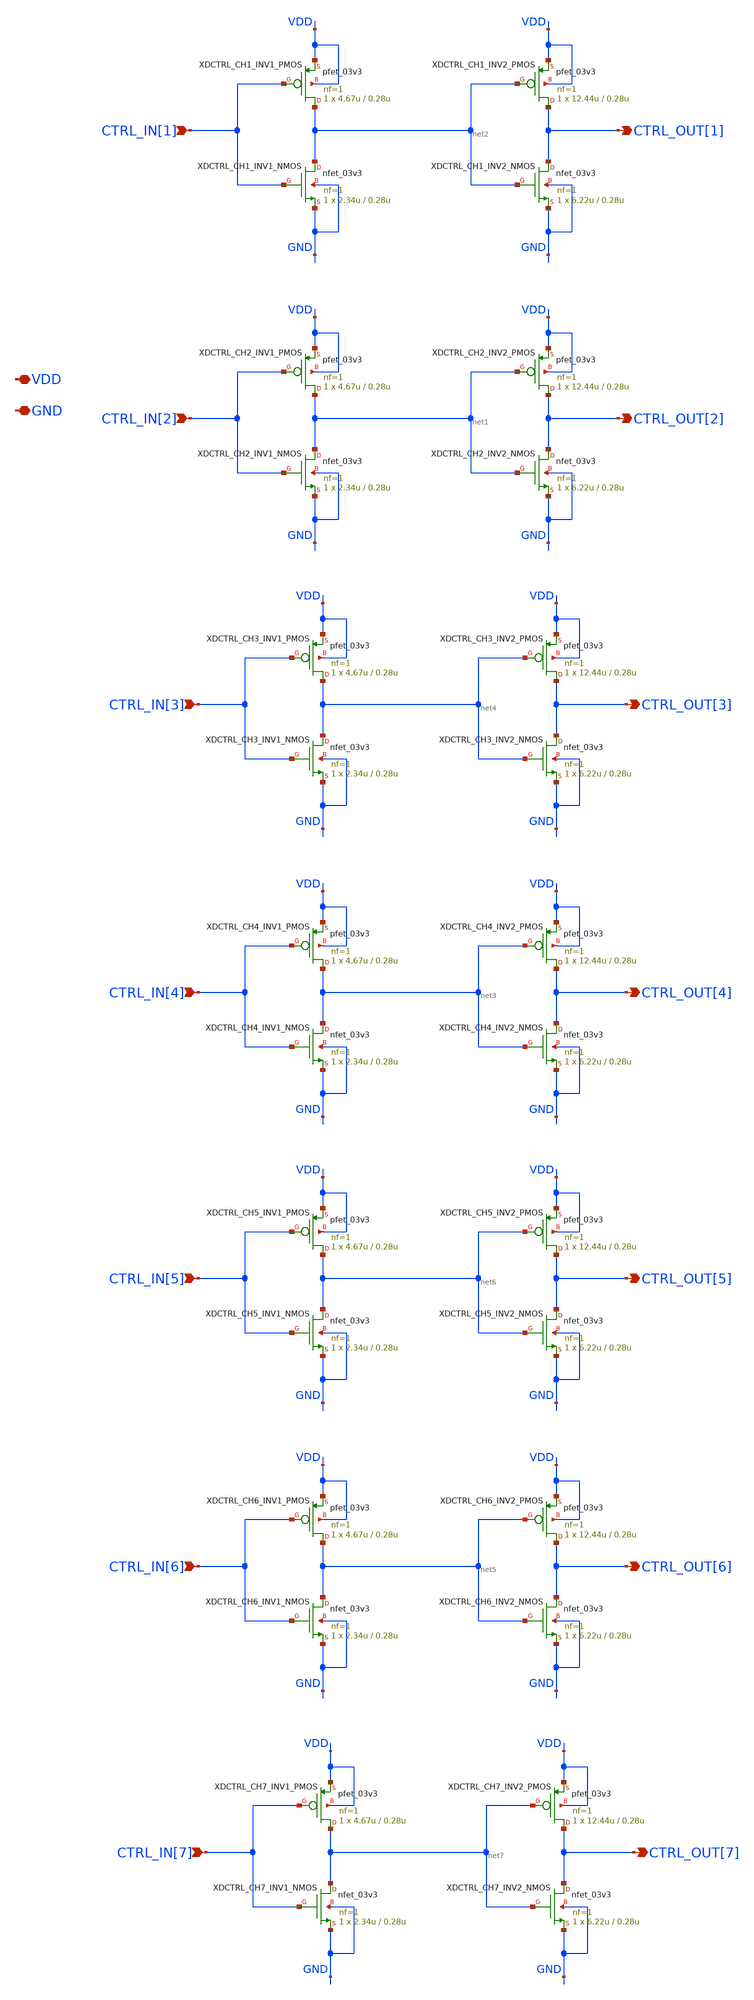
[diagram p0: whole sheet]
** sch_path: verification/a44_w5p29_trans_driver/01_CURRENT_CIRCUIT_FILES/xschem/A44_CONVERSION_BUFFER.sch
**.subckt A44_CONVERSION_BUFFER CTRL_IN[2] CTRL_OUT[2] VDD GND CTRL_IN[1] CTRL_OUT[1] CTRL_IN[4]
*+ CTRL_OUT[4] CTRL_IN[3] CTRL_OUT[3] CTRL_IN[6] CTRL_OUT[6] CTRL_IN[5] CTRL_OUT[5] CTRL_IN[7] CTRL_OUT[7]
*.ipin CTRL_IN[2]
*.opin CTRL_OUT[2]
*.iopin VDD
*.iopin GND
*.ipin CTRL_IN[1]
*.opin CTRL_OUT[1]
*.ipin CTRL_IN[4]
*.opin CTRL_OUT[4]
*.ipin CTRL_IN[3]
*.opin CTRL_OUT[3]
*.ipin CTRL_IN[6]
*.opin CTRL_OUT[6]
*.ipin CTRL_IN[5]
*.opin CTRL_OUT[5]
*.ipin CTRL_IN[7]
*.opin CTRL_OUT[7]
XDCTRL_CH2_INV1_NMOS net1 CTRL_IN[2] GND GND nfet_03v3 L=0.28u W=2.34u nf=1 ad='int((nf+1)/2) * W/nf * 0.18u'
+ as='int((nf+2)/2) * W/nf * 0.18u' pd='2*int((nf+1)/2) * (W/nf + 0.18u)' ps='2*int((nf+2)/2) * (W/nf + 0.18u)'
+ nrd='0.18u / W' nrs='0.18u / W' sa=0 sb=0 sd=0 m=1
XDCTRL_CH2_INV1_PMOS net1 CTRL_IN[2] VDD VDD pfet_03v3 L=0.28u W=4.67u nf=1 ad='int((nf+1)/2) * W/nf * 0.18u'
+ as='int((nf+2)/2) * W/nf * 0.18u' pd='2*int((nf+1)/2) * (W/nf + 0.18u)' ps='2*int((nf+2)/2) * (W/nf + 0.18u)'
+ nrd='0.18u / W' nrs='0.18u / W' sa=0 sb=0 sd=0 m=1
XDCTRL_CH2_INV2_NMOS CTRL_OUT[2] net1 GND GND nfet_03v3 L=0.28u W=6.22u nf=1 ad='int((nf+1)/2) * W/nf * 0.18u'
+ as='int((nf+2)/2) * W/nf * 0.18u' pd='2*int((nf+1)/2) * (W/nf + 0.18u)' ps='2*int((nf+2)/2) * (W/nf + 0.18u)'
+ nrd='0.18u / W' nrs='0.18u / W' sa=0 sb=0 sd=0 m=1
XDCTRL_CH2_INV2_PMOS CTRL_OUT[2] net1 VDD VDD pfet_03v3 L=0.28u W=12.44u nf=1 ad='int((nf+1)/2) * W/nf * 0.18u'
+ as='int((nf+2)/2) * W/nf * 0.18u' pd='2*int((nf+1)/2) * (W/nf + 0.18u)' ps='2*int((nf+2)/2) * (W/nf + 0.18u)'
+ nrd='0.18u / W' nrs='0.18u / W' sa=0 sb=0 sd=0 m=1
XDCTRL_CH1_INV1_NMOS net2 CTRL_IN[1] GND GND nfet_03v3 L=0.28u W=2.34u nf=1 ad='int((nf+1)/2) * W/nf * 0.18u'
+ as='int((nf+2)/2) * W/nf * 0.18u' pd='2*int((nf+1)/2) * (W/nf + 0.18u)' ps='2*int((nf+2)/2) * (W/nf + 0.18u)'
+ nrd='0.18u / W' nrs='0.18u / W' sa=0 sb=0 sd=0 m=1
XDCTRL_CH1_INV1_PMOS net2 CTRL_IN[1] VDD VDD pfet_03v3 L=0.28u W=4.67u nf=1 ad='int((nf+1)/2) * W/nf * 0.18u'
+ as='int((nf+2)/2) * W/nf * 0.18u' pd='2*int((nf+1)/2) * (W/nf + 0.18u)' ps='2*int((nf+2)/2) * (W/nf + 0.18u)'
+ nrd='0.18u / W' nrs='0.18u / W' sa=0 sb=0 sd=0 m=1
XDCTRL_CH1_INV2_NMOS CTRL_OUT[1] net2 GND GND nfet_03v3 L=0.28u W=6.22u nf=1 ad='int((nf+1)/2) * W/nf * 0.18u'
+ as='int((nf+2)/2) * W/nf * 0.18u' pd='2*int((nf+1)/2) * (W/nf + 0.18u)' ps='2*int((nf+2)/2) * (W/nf + 0.18u)'
+ nrd='0.18u / W' nrs='0.18u / W' sa=0 sb=0 sd=0 m=1
XDCTRL_CH1_INV2_PMOS CTRL_OUT[1] net2 VDD VDD pfet_03v3 L=0.28u W=12.44u nf=1 ad='int((nf+1)/2) * W/nf * 0.18u'
+ as='int((nf+2)/2) * W/nf * 0.18u' pd='2*int((nf+1)/2) * (W/nf + 0.18u)' ps='2*int((nf+2)/2) * (W/nf + 0.18u)'
+ nrd='0.18u / W' nrs='0.18u / W' sa=0 sb=0 sd=0 m=1
XDCTRL_CH4_INV1_NMOS net3 CTRL_IN[4] GND GND nfet_03v3 L=0.28u W=2.34u nf=1 ad='int((nf+1)/2) * W/nf * 0.18u'
+ as='int((nf+2)/2) * W/nf * 0.18u' pd='2*int((nf+1)/2) * (W/nf + 0.18u)' ps='2*int((nf+2)/2) * (W/nf + 0.18u)'
+ nrd='0.18u / W' nrs='0.18u / W' sa=0 sb=0 sd=0 m=1
XDCTRL_CH4_INV1_PMOS net3 CTRL_IN[4] VDD VDD pfet_03v3 L=0.28u W=4.67u nf=1 ad='int((nf+1)/2) * W/nf * 0.18u'
+ as='int((nf+2)/2) * W/nf * 0.18u' pd='2*int((nf+1)/2) * (W/nf + 0.18u)' ps='2*int((nf+2)/2) * (W/nf + 0.18u)'
+ nrd='0.18u / W' nrs='0.18u / W' sa=0 sb=0 sd=0 m=1
XDCTRL_CH4_INV2_NMOS CTRL_OUT[4] net3 GND GND nfet_03v3 L=0.28u W=6.22u nf=1 ad='int((nf+1)/2) * W/nf * 0.18u'
+ as='int((nf+2)/2) * W/nf * 0.18u' pd='2*int((nf+1)/2) * (W/nf + 0.18u)' ps='2*int((nf+2)/2) * (W/nf + 0.18u)'
+ nrd='0.18u / W' nrs='0.18u / W' sa=0 sb=0 sd=0 m=1
XDCTRL_CH4_INV2_PMOS CTRL_OUT[4] net3 VDD VDD pfet_03v3 L=0.28u W=12.44u nf=1 ad='int((nf+1)/2) * W/nf * 0.18u'
+ as='int((nf+2)/2) * W/nf * 0.18u' pd='2*int((nf+1)/2) * (W/nf + 0.18u)' ps='2*int((nf+2)/2) * (W/nf + 0.18u)'
+ nrd='0.18u / W' nrs='0.18u / W' sa=0 sb=0 sd=0 m=1
XDCTRL_CH3_INV1_NMOS net4 CTRL_IN[3] GND GND nfet_03v3 L=0.28u W=2.34u nf=1 ad='int((nf+1)/2) * W/nf * 0.18u'
+ as='int((nf+2)/2) * W/nf * 0.18u' pd='2*int((nf+1)/2) * (W/nf + 0.18u)' ps='2*int((nf+2)/2) * (W/nf + 0.18u)'
+ nrd='0.18u / W' nrs='0.18u / W' sa=0 sb=0 sd=0 m=1
XDCTRL_CH3_INV1_PMOS net4 CTRL_IN[3] VDD VDD pfet_03v3 L=0.28u W=4.67u nf=1 ad='int((nf+1)/2) * W/nf * 0.18u'
+ as='int((nf+2)/2) * W/nf * 0.18u' pd='2*int((nf+1)/2) * (W/nf + 0.18u)' ps='2*int((nf+2)/2) * (W/nf + 0.18u)'
+ nrd='0.18u / W' nrs='0.18u / W' sa=0 sb=0 sd=0 m=1
XDCTRL_CH3_INV2_NMOS CTRL_OUT[3] net4 GND GND nfet_03v3 L=0.28u W=6.22u nf=1 ad='int((nf+1)/2) * W/nf * 0.18u'
+ as='int((nf+2)/2) * W/nf * 0.18u' pd='2*int((nf+1)/2) * (W/nf + 0.18u)' ps='2*int((nf+2)/2) * (W/nf + 0.18u)'
+ nrd='0.18u / W' nrs='0.18u / W' sa=0 sb=0 sd=0 m=1
XDCTRL_CH3_INV2_PMOS CTRL_OUT[3] net4 VDD VDD pfet_03v3 L=0.28u W=12.44u nf=1 ad='int((nf+1)/2) * W/nf * 0.18u'
+ as='int((nf+2)/2) * W/nf * 0.18u' pd='2*int((nf+1)/2) * (W/nf + 0.18u)' ps='2*int((nf+2)/2) * (W/nf + 0.18u)'
+ nrd='0.18u / W' nrs='0.18u / W' sa=0 sb=0 sd=0 m=1
XDCTRL_CH6_INV1_NMOS net5 CTRL_IN[6] GND GND nfet_03v3 L=0.28u W=2.34u nf=1 ad='int((nf+1)/2) * W/nf * 0.18u'
+ as='int((nf+2)/2) * W/nf * 0.18u' pd='2*int((nf+1)/2) * (W/nf + 0.18u)' ps='2*int((nf+2)/2) * (W/nf + 0.18u)'
+ nrd='0.18u / W' nrs='0.18u / W' sa=0 sb=0 sd=0 m=1
XDCTRL_CH6_INV1_PMOS net5 CTRL_IN[6] VDD VDD pfet_03v3 L=0.28u W=4.67u nf=1 ad='int((nf+1)/2) * W/nf * 0.18u'
+ as='int((nf+2)/2) * W/nf * 0.18u' pd='2*int((nf+1)/2) * (W/nf + 0.18u)' ps='2*int((nf+2)/2) * (W/nf + 0.18u)'
+ nrd='0.18u / W' nrs='0.18u / W' sa=0 sb=0 sd=0 m=1
XDCTRL_CH6_INV2_NMOS CTRL_OUT[6] net5 GND GND nfet_03v3 L=0.28u W=6.22u nf=1 ad='int((nf+1)/2) * W/nf * 0.18u'
+ as='int((nf+2)/2) * W/nf * 0.18u' pd='2*int((nf+1)/2) * (W/nf + 0.18u)' ps='2*int((nf+2)/2) * (W/nf + 0.18u)'
+ nrd='0.18u / W' nrs='0.18u / W' sa=0 sb=0 sd=0 m=1
XDCTRL_CH6_INV2_PMOS CTRL_OUT[6] net5 VDD VDD pfet_03v3 L=0.28u W=12.44u nf=1 ad='int((nf+1)/2) * W/nf * 0.18u'
+ as='int((nf+2)/2) * W/nf * 0.18u' pd='2*int((nf+1)/2) * (W/nf + 0.18u)' ps='2*int((nf+2)/2) * (W/nf + 0.18u)'
+ nrd='0.18u / W' nrs='0.18u / W' sa=0 sb=0 sd=0 m=1
XDCTRL_CH5_INV1_NMOS net6 CTRL_IN[5] GND GND nfet_03v3 L=0.28u W=2.34u nf=1 ad='int((nf+1)/2) * W/nf * 0.18u'
+ as='int((nf+2)/2) * W/nf * 0.18u' pd='2*int((nf+1)/2) * (W/nf + 0.18u)' ps='2*int((nf+2)/2) * (W/nf + 0.18u)'
+ nrd='0.18u / W' nrs='0.18u / W' sa=0 sb=0 sd=0 m=1
XDCTRL_CH5_INV1_PMOS net6 CTRL_IN[5] VDD VDD pfet_03v3 L=0.28u W=4.67u nf=1 ad='int((nf+1)/2) * W/nf * 0.18u'
+ as='int((nf+2)/2) * W/nf * 0.18u' pd='2*int((nf+1)/2) * (W/nf + 0.18u)' ps='2*int((nf+2)/2) * (W/nf + 0.18u)'
+ nrd='0.18u / W' nrs='0.18u / W' sa=0 sb=0 sd=0 m=1
XDCTRL_CH5_INV2_NMOS CTRL_OUT[5] net6 GND GND nfet_03v3 L=0.28u W=6.22u nf=1 ad='int((nf+1)/2) * W/nf * 0.18u'
+ as='int((nf+2)/2) * W/nf * 0.18u' pd='2*int((nf+1)/2) * (W/nf + 0.18u)' ps='2*int((nf+2)/2) * (W/nf + 0.18u)'
+ nrd='0.18u / W' nrs='0.18u / W' sa=0 sb=0 sd=0 m=1
XDCTRL_CH5_INV2_PMOS CTRL_OUT[5] net6 VDD VDD pfet_03v3 L=0.28u W=12.44u nf=1 ad='int((nf+1)/2) * W/nf * 0.18u'
+ as='int((nf+2)/2) * W/nf * 0.18u' pd='2*int((nf+1)/2) * (W/nf + 0.18u)' ps='2*int((nf+2)/2) * (W/nf + 0.18u)'
+ nrd='0.18u / W' nrs='0.18u / W' sa=0 sb=0 sd=0 m=1
XDCTRL_CH7_INV1_NMOS net7 CTRL_IN[7] GND GND nfet_03v3 L=0.28u W=2.34u nf=1 ad='int((nf+1)/2) * W/nf * 0.18u'
+ as='int((nf+2)/2) * W/nf * 0.18u' pd='2*int((nf+1)/2) * (W/nf + 0.18u)' ps='2*int((nf+2)/2) * (W/nf + 0.18u)'
+ nrd='0.18u / W' nrs='0.18u / W' sa=0 sb=0 sd=0 m=1
XDCTRL_CH7_INV1_PMOS net7 CTRL_IN[7] VDD VDD pfet_03v3 L=0.28u W=4.67u nf=1 ad='int((nf+1)/2) * W/nf * 0.18u'
+ as='int((nf+2)/2) * W/nf * 0.18u' pd='2*int((nf+1)/2) * (W/nf + 0.18u)' ps='2*int((nf+2)/2) * (W/nf + 0.18u)'
+ nrd='0.18u / W' nrs='0.18u / W' sa=0 sb=0 sd=0 m=1
XDCTRL_CH7_INV2_NMOS CTRL_OUT[7] net7 GND GND nfet_03v3 L=0.28u W=6.22u nf=1 ad='int((nf+1)/2) * W/nf * 0.18u'
+ as='int((nf+2)/2) * W/nf * 0.18u' pd='2*int((nf+1)/2) * (W/nf + 0.18u)' ps='2*int((nf+2)/2) * (W/nf + 0.18u)'
+ nrd='0.18u / W' nrs='0.18u / W' sa=0 sb=0 sd=0 m=1
XDCTRL_CH7_INV2_PMOS CTRL_OUT[7] net7 VDD VDD pfet_03v3 L=0.28u W=12.44u nf=1 ad='int((nf+1)/2) * W/nf * 0.18u'
+ as='int((nf+2)/2) * W/nf * 0.18u' pd='2*int((nf+1)/2) * (W/nf + 0.18u)' ps='2*int((nf+2)/2) * (W/nf + 0.18u)'
+ nrd='0.18u / W' nrs='0.18u / W' sa=0 sb=0 sd=0 m=1
**.ends
.end
